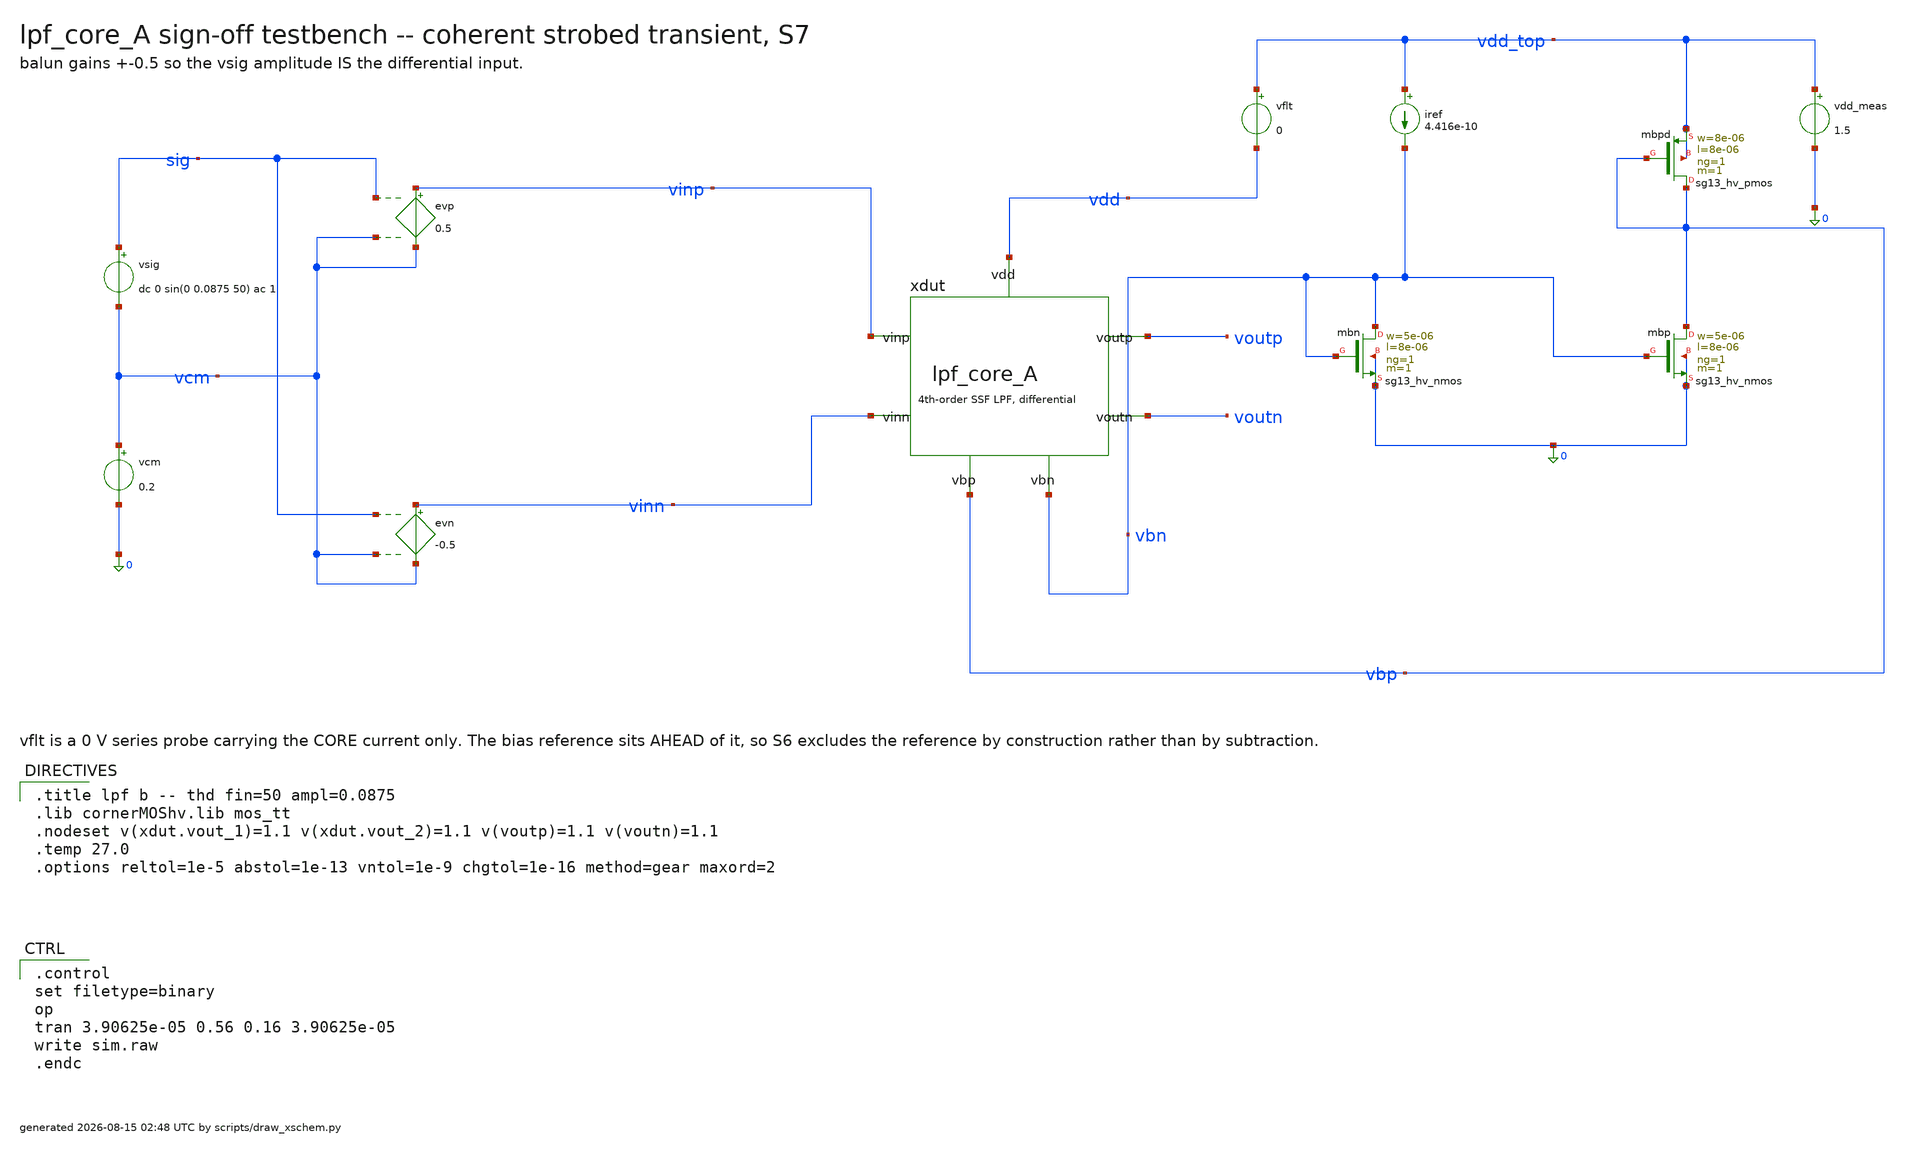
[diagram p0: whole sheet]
** sch_path: signoff/A-minarea/lpf_tb_A_thd.sch
**.subckt lpf_tb_A_thd
vsig sig vcm dc 0 sin(0 0.0875 50) ac 1
vcm vcm 0 0.2
evp vinp vcm sig vcm 0.5
evn vinn vcm sig vcm -0.5
xdut vinp vinn voutp voutn vbn vbp vdd lpf_core_A
vflt vdd_top vdd 0
vdd_meas vdd_top 0 1.5
iref vdd_top vbn 4.416e-10
Xmbn vbn vbn 0 0 sg13_hv_nmos w=5e-06 l=8e-06 ng=1 m=1 mm_ok=1
Xmbp vbp vbn 0 0 sg13_hv_nmos w=5e-06 l=8e-06 ng=1 m=1 mm_ok=1
Xmbpd vbp vbp vdd_top vdd_top sg13_hv_pmos w=8e-06 l=8e-06 ng=1 m=1 mm_ok=1
**** begin user architecture code

.title lpf b -- thd fin=50 ampl=0.0875
.lib cornerMOShv.lib mos_tt
.nodeset v(xdut.vout_1)=1.1 v(xdut.vout_2)=1.1 v(voutp)=1.1 v(voutn)=1.1
.temp 27.0
.options reltol=1e-5 abstol=1e-13 vntol=1e-9 chgtol=1e-16 method=gear maxord=2


.control
set filetype=binary
op
tran 3.90625e-05 0.56 0.16 3.90625e-05
write sim.raw
.endc

**** end user architecture code
**.ends
.end
